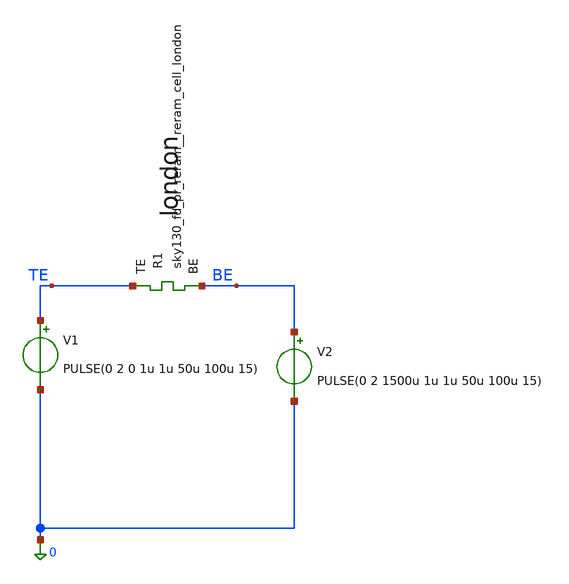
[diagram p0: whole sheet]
** sch_path: memristor_models/rram_london/tb_pulses_uk.sch
**.subckt tb_pulses_uk
V1 TE 0 PULSE(0 2 0 1u 1u 50u 100u 15)
V2 BE 0 PULSE(0 2 1500u 1u 1u 50u 100u 15)
XR1 TE BE sky130_fd_pr_reram__reram_cell_london
**** begin user architecture code

** opencircuitdesign pdks install

.inc $::SKYWATER_MODELS/rram_v0.spice



.option savecurrents
.tran 1u 3m
.control
	save all
	run
	write tb_pulses_uk.raw
.endc



**** end user architecture code
**.ends
.end
